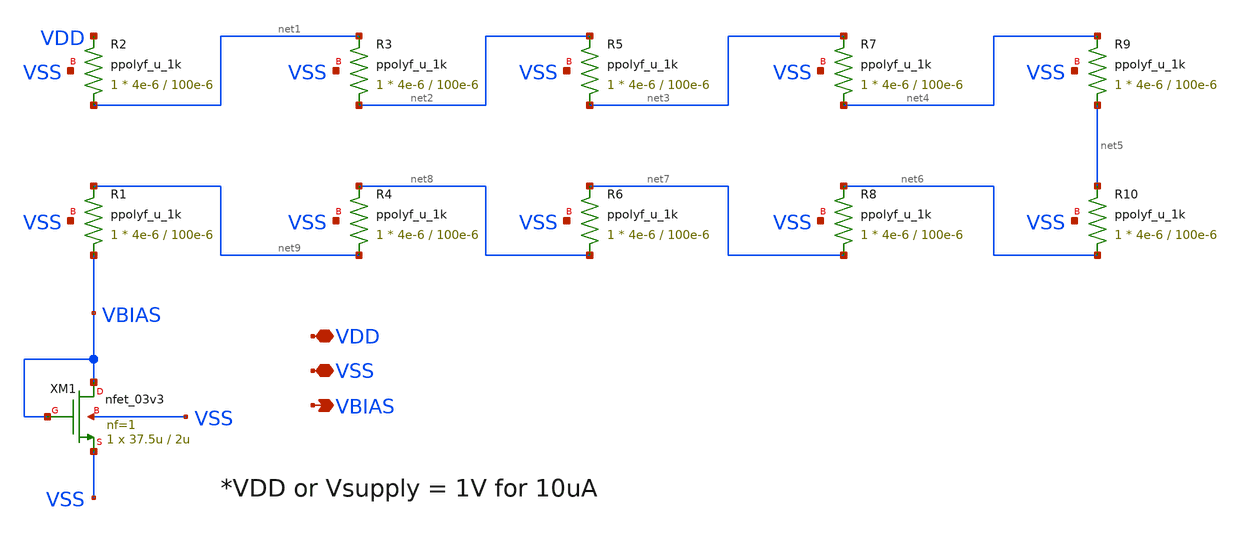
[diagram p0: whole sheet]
** sch_path: w1_advanced-foundation/w1_task/w1_current_mirror/n-bias-gen.sch
**.subckt n-bias-gen VDD VSS VBIAS
*.iopin VDD
*.iopin VSS
*.opin VBIAS
XM1 VBIAS VBIAS VSS VSS nfet_03v3 L=2u W=37.5u nf=1 ad='int((nf+1)/2) * W/nf * 0.18u' as='int((nf+2)/2) * W/nf * 0.18u'
+ pd='2*int((nf+1)/2) * (W/nf + 0.18u)' ps='2*int((nf+2)/2) * (W/nf + 0.18u)' nrd='0.18u / W' nrs='0.18u / W'
+ sa=0 sb=0 sd=0 m=1
XR1 VBIAS net9 VSS ppolyf_u_1k r_width=4e-6 r_length=100e-6 m=1
XR2 net1 VDD VSS ppolyf_u_1k r_width=4e-6 r_length=100e-6 m=1
XR3 net2 net1 VSS ppolyf_u_1k r_width=4e-6 r_length=100e-6 m=1
XR4 net9 net8 VSS ppolyf_u_1k r_width=4e-6 r_length=100e-6 m=1
XR5 net3 net2 VSS ppolyf_u_1k r_width=4e-6 r_length=100e-6 m=1
XR6 net8 net7 VSS ppolyf_u_1k r_width=4e-6 r_length=100e-6 m=1
XR7 net4 net3 VSS ppolyf_u_1k r_width=4e-6 r_length=100e-6 m=1
XR8 net7 net6 VSS ppolyf_u_1k r_width=4e-6 r_length=100e-6 m=1
XR9 net5 net4 VSS ppolyf_u_1k r_width=4e-6 r_length=100e-6 m=1
XR10 net6 net5 VSS ppolyf_u_1k r_width=4e-6 r_length=100e-6 m=1
**.ends
.end
